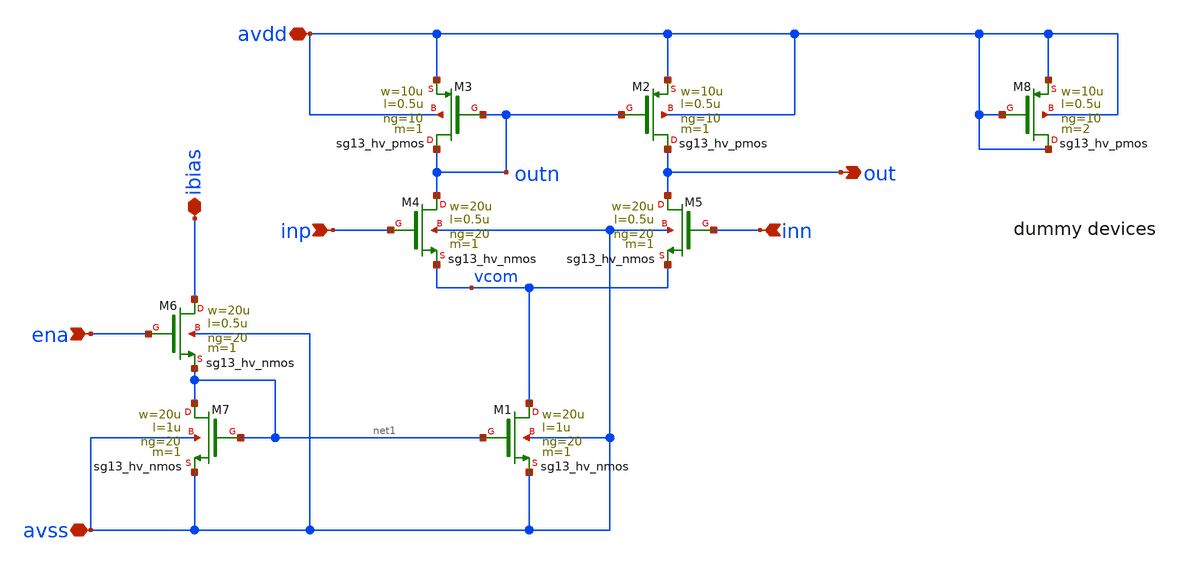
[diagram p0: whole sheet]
** sch_path: xschem/n_amp_large.sch
**.subckt n_amp_large inp inn out avdd avss ena ibias
*.ipin inp
*.ipin inn
*.opin out
*.iopin avdd
*.iopin avss
*.ipin ena
*.iopin ibias
XM1 vcom net1 avss avss sg13_hv_nmos w=20u l=1u ng=20 m=1 mm_ok=1
XM2 out outn avdd avdd sg13_hv_pmos w=10u l=0.5u ng=10 m=1 mm_ok=1
XM3 outn outn avdd avdd sg13_hv_pmos w=10u l=0.5u ng=10 m=1 mm_ok=1
XM4 outn inp vcom avss sg13_hv_nmos w=20u l=0.5u ng=20 m=1 mm_ok=1
XM5 out inn vcom avss sg13_hv_nmos w=20u l=0.5u ng=20 m=1 mm_ok=1
XM6 ibias ena net1 avss sg13_hv_nmos w=20u l=0.5u ng=20 m=1 mm_ok=1
XM7 net1 net1 avss avss sg13_hv_nmos w=20u l=1u ng=20 m=1 mm_ok=1
XM8 avdd avdd avdd avdd sg13_hv_pmos w=10u l=0.5u ng=10 m=2 mm_ok=1
**.ends
.end
